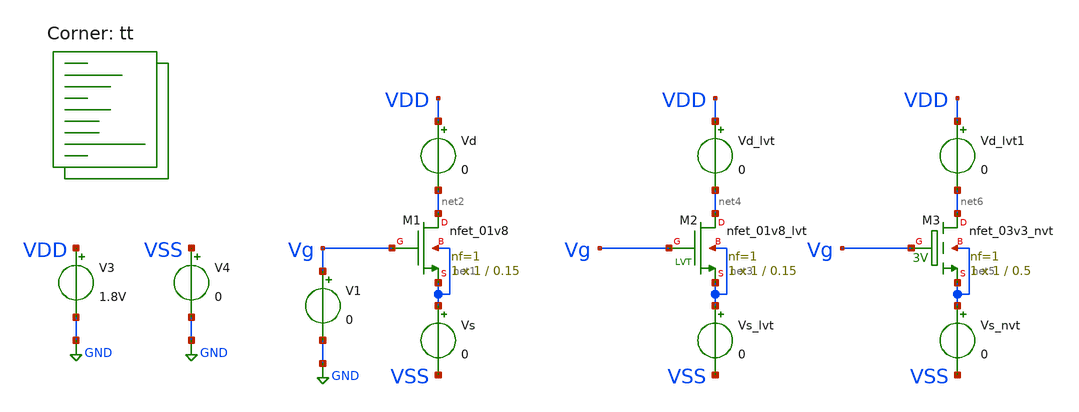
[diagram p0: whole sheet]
** sch_path: xschem/tests/dummy_tests/nmos_lvt.sch
**.subckt nmos_lvt
V3 VDD GND 1.8V
V4 VSS GND 0
XM1 net2 Vg net1 net1 sky130_fd_pr__nfet_01v8 L=0.15 W=1 nf=1 ad='int((nf+1)/2) * W/nf * 0.29' as='int((nf+2)/2) * W/nf * 0.29'
+ pd='2*int((nf+1)/2) * (W/nf + 0.29)' ps='2*int((nf+2)/2) * (W/nf + 0.29)' nrd='0.29 / W' nrs='0.29 / W'
+ sa=0 sb=0 sd=0 mult=1 m=1
V1 Vg GND 0
Vd VDD net2 0
Vs net1 VSS 0
XM2 net4 Vg net3 net3 sky130_fd_pr__nfet_01v8_lvt L=0.15 W=1 nf=1 ad='int((nf+1)/2) * W/nf * 0.29' as='int((nf+2)/2) * W/nf * 0.29'
+ pd='2*int((nf+1)/2) * (W/nf + 0.29)' ps='2*int((nf+2)/2) * (W/nf + 0.29)' nrd='0.29 / W' nrs='0.29 / W'
+ sa=0 sb=0 sd=0 mult=1 m=1
Vd_lvt VDD net4 0
Vs_lvt net3 VSS 0
XM3 net6 Vg net5 net5 sky130_fd_pr__nfet_03v3_nvt L=0.5 W=1 nf=1 ad='int((nf+1)/2) * W/nf * 0.29' as='int((nf+2)/2) * W/nf * 0.29'
+ pd='2*int((nf+1)/2) * (W/nf + 0.29)' ps='2*int((nf+2)/2) * (W/nf + 0.29)' nrd='0.29 / W' nrs='0.29 / W'
+ sa=0 sb=0 sd=0 mult=1 m=1
Vd_lvt1 VDD net6 0
Vs_nvt net5 VSS 0
**** begin user architecture code
 *.lib $::SKYWATER_MODELS/sky130.lib.spice tt
.include $::SKYWATER_STDCELLS/sky130_fd_sc_hd.spice


.options acct list
.temp 25
*vvcc VDD 0 dc 1.8
*vvss VSS 0 0
.control
*tran 0.1u 400u
dc v1 0 1.8V 0.05
*plot RST_PLS clk+2 Pulse+4
plot Vg-Vss
plot i(Vs) i(Vs_lvt) i(vs_nvt)
write pulse_generator_test.raw
.endc


.lib $::SKYWATER_MODELS/sky130.lib.spice tt
**** end user architecture code
**.ends
.GLOBAL GND
.end
